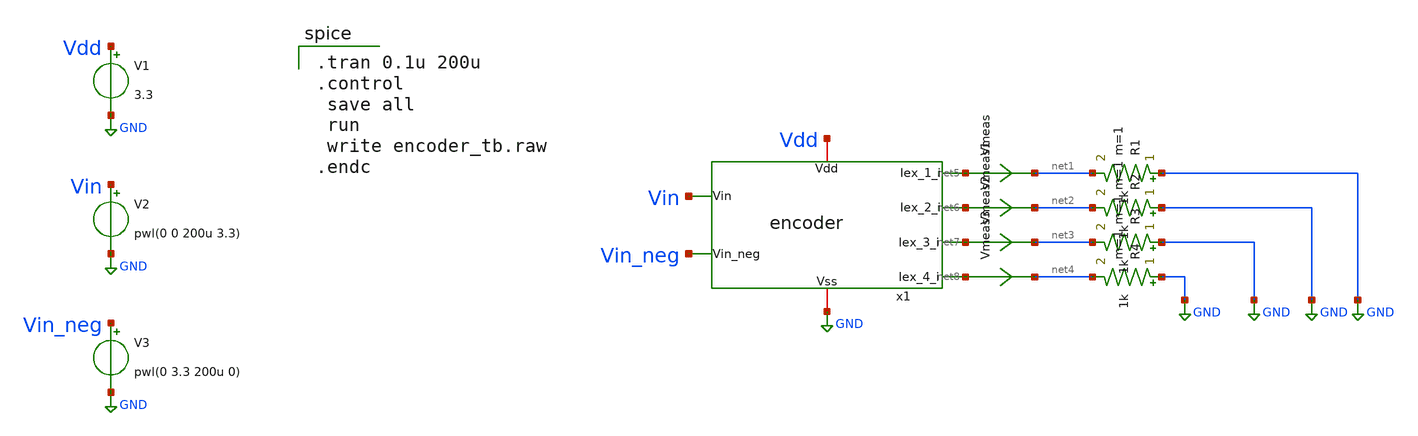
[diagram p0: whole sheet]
** sch_path: designs/libs/snn_analog/encoder/sch/encoder_tb.sch
**.subckt encoder_tb
x1 Vdd GND Vin Vin_neg net5 net6 net7 net8 encoder
V1 Vdd GND 3.3
V2 Vin GND pwl(0 0 200u 3.3)
V3 Vin_neg GND pwl(0 3.3 200u 0)
R1 GND net1 1k m=1
R2 GND net2 1k m=1
R3 GND net3 1k m=1
R4 GND net4 1k m=1
Vmeas net5 net1 0
.save i(vmeas)
Vmeas1 net6 net2 0
.save i(vmeas1)
Vmeas2 net7 net3 0
.save i(vmeas2)
Vmeas3 net8 net4 0
.save i(vmeas3)
**** begin user architecture code

.include $::180MCU_MODELS/design.ngspice
.lib $::180MCU_MODELS/sm141064.ngspice typical


.tran 0.1u 200u
.control
 save all
 run
 write encoder_tb.raw
.endc

**** end user architecture code
**.ends

* expanding   symbol:  encoder.sym # of pins=8
** sym_path: designs/libs/snn_analog/encoder/sch/encoder.sym
** sch_path: designs/libs/snn_analog/encoder/sch/encoder.sch
.subckt encoder Vdd Vss Vin Vin_neg Iex_1_i Iex_2_i Iex_3_i Iex_4_i
*.iopin Vdd
*.iopin Vss
*.ipin Vin
*.ipin Vin_neg
*.opin Iex_1_i
*.opin Iex_4_i
*.opin Iex_2_i
*.opin Iex_3_i
XM1 x Vin a Vss nfet_03v3 L=10u W=0.5u nf=1 ad='int((nf+1)/2) * W/nf * 0.18u' as='int((nf+2)/2) * W/nf * 0.18u'
+ pd='2*int((nf+1)/2) * (W/nf + 0.18u)' ps='2*int((nf+2)/2) * (W/nf + 0.18u)' nrd='0.18u / W' nrs='0.18u / W'
+ sa=0 sb=0 sd=0 m=1
XM2 y Vin_neg a Vss nfet_03v3 L=10u W=0.5u nf=1 ad='int((nf+1)/2) * W/nf * 0.18u' as='int((nf+2)/2) * W/nf * 0.18u'
+ pd='2*int((nf+1)/2) * (W/nf + 0.18u)' ps='2*int((nf+2)/2) * (W/nf + 0.18u)' nrd='0.18u / W' nrs='0.18u / W'
+ sa=0 sb=0 sd=0 m=1
XM3 x x Vdd Vdd pfet_03v3 L=0.28u W=2u nf=1 ad='int((nf+1)/2) * W/nf * 0.18u' as='int((nf+2)/2) * W/nf * 0.18u'
+ pd='2*int((nf+1)/2) * (W/nf + 0.18u)' ps='2*int((nf+2)/2) * (W/nf + 0.18u)' nrd='0.18u / W' nrs='0.18u / W'
+ sa=0 sb=0 sd=0 m=1
XM4 y y Vdd Vdd pfet_03v3 L=0.28u W=2u nf=1 ad='int((nf+1)/2) * W/nf * 0.18u' as='int((nf+2)/2) * W/nf * 0.18u'
+ pd='2*int((nf+1)/2) * (W/nf + 0.18u)' ps='2*int((nf+2)/2) * (W/nf + 0.18u)' nrd='0.18u / W' nrs='0.18u / W'
+ sa=0 sb=0 sd=0 m=1
XM5 Iex_2_i x Vdd Vdd pfet_03v3 L=1.86u W=0.93u nf=1 ad='int((nf+1)/2) * W/nf * 0.18u' as='int((nf+2)/2) * W/nf * 0.18u'
+ pd='2*int((nf+1)/2) * (W/nf + 0.18u)' ps='2*int((nf+2)/2) * (W/nf + 0.18u)' nrd='0.18u / W' nrs='0.18u / W'
+ sa=0 sb=0 sd=0 m=1
XM7 Iex_3_i y Vdd Vdd pfet_03v3 L=1.86u W=0.93u nf=1 ad='int((nf+1)/2) * W/nf * 0.18u' as='int((nf+2)/2) * W/nf * 0.18u'
+ pd='2*int((nf+1)/2) * (W/nf + 0.18u)' ps='2*int((nf+2)/2) * (W/nf + 0.18u)' nrd='0.18u / W' nrs='0.18u / W'
+ sa=0 sb=0 sd=0 m=1
XM9 a net1 Vss Vss nfet_03v3 L=0.28u W=0.5u nf=1 ad='int((nf+1)/2) * W/nf * 0.18u' as='int((nf+2)/2) * W/nf * 0.18u'
+ pd='2*int((nf+1)/2) * (W/nf + 0.18u)' ps='2*int((nf+2)/2) * (W/nf + 0.18u)' nrd='0.18u / W' nrs='0.18u / W'
+ sa=0 sb=0 sd=0 m=1
XM10 net1 net1 Vss Vss nfet_03v3 L=0.28u W=0.5u nf=1 ad='int((nf+1)/2) * W/nf * 0.18u' as='int((nf+2)/2) * W/nf * 0.18u'
+ pd='2*int((nf+1)/2) * (W/nf + 0.18u)' ps='2*int((nf+2)/2) * (W/nf + 0.18u)' nrd='0.18u / W' nrs='0.18u / W'
+ sa=0 sb=0 sd=0 m=1
XM11 net1 net1 Vdd Vdd pfet_03v3 L=0.28u W=0.5u nf=1 ad='int((nf+1)/2) * W/nf * 0.18u' as='int((nf+2)/2) * W/nf * 0.18u'
+ pd='2*int((nf+1)/2) * (W/nf + 0.18u)' ps='2*int((nf+2)/2) * (W/nf + 0.18u)' nrd='0.18u / W' nrs='0.18u / W'
+ sa=0 sb=0 sd=0 m=1
XM6 Iex_4_i y Vdd Vdd pfet_03v3 L=1.86u W=0.93u nf=1 ad='int((nf+1)/2) * W/nf * 0.18u' as='int((nf+2)/2) * W/nf * 0.18u'
+ pd='2*int((nf+1)/2) * (W/nf + 0.18u)' ps='2*int((nf+2)/2) * (W/nf + 0.18u)' nrd='0.18u / W' nrs='0.18u / W'
+ sa=0 sb=0 sd=0 m=1
XM8 Iex_1_i x Vdd Vdd pfet_03v3 L=1.86u W=0.93u nf=1 ad='int((nf+1)/2) * W/nf * 0.18u' as='int((nf+2)/2) * W/nf * 0.18u'
+ pd='2*int((nf+1)/2) * (W/nf + 0.18u)' ps='2*int((nf+2)/2) * (W/nf + 0.18u)' nrd='0.18u / W' nrs='0.18u / W'
+ sa=0 sb=0 sd=0 m=1
.ends

.GLOBAL GND
.end
